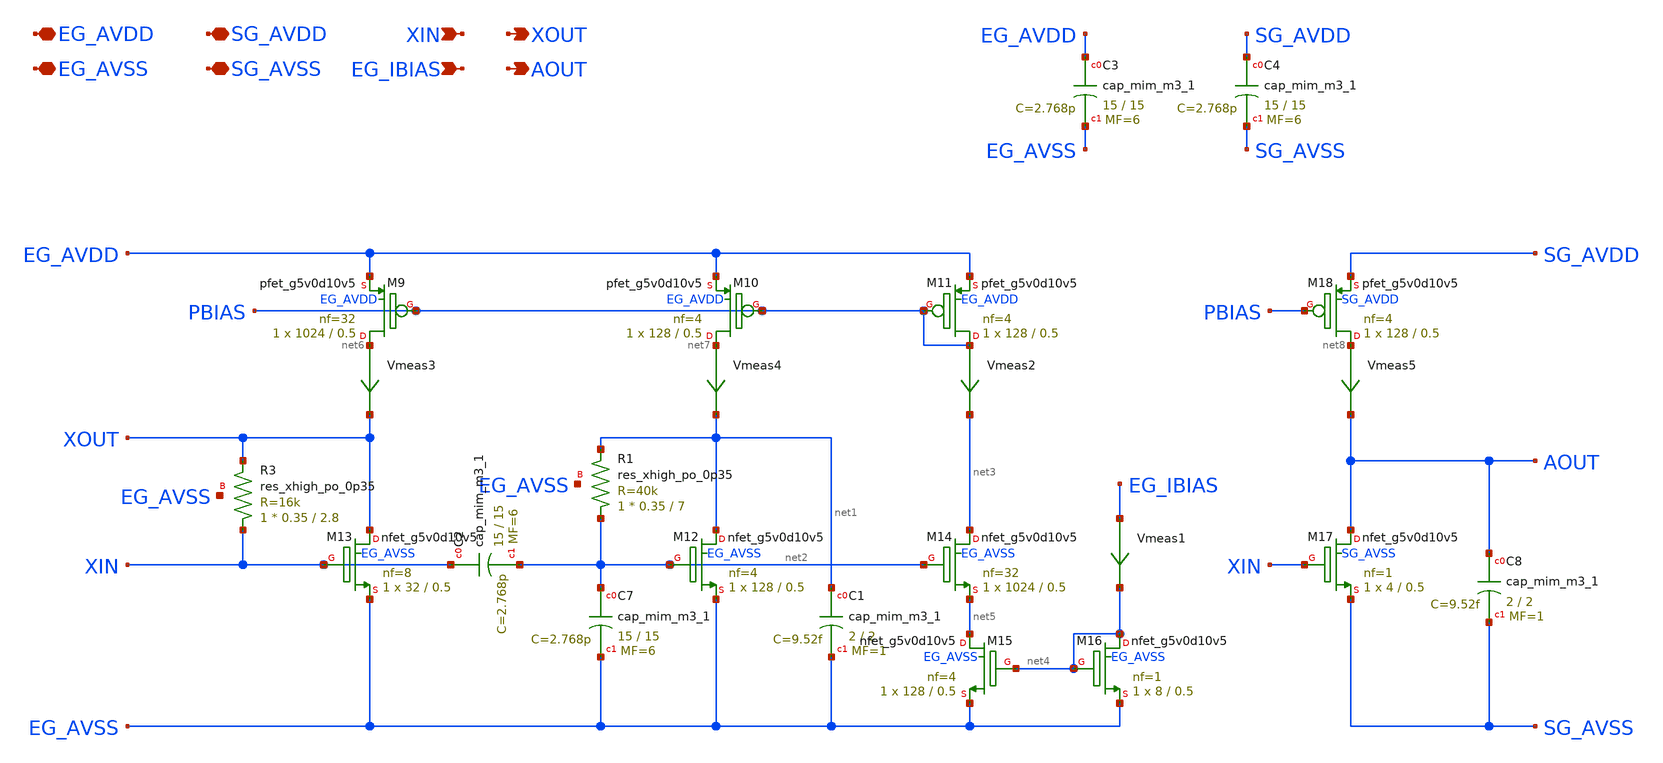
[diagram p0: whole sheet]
** sch_path: xschem/vittoz_pierce_osc.sch
**.subckt vittoz_pierce_osc EG_AVDD EG_AVSS SG_AVDD SG_AVSS XIN EG_IBIAS XOUT AOUT
*.iopin EG_AVDD
*.iopin EG_AVSS
*.iopin SG_AVDD
*.iopin SG_AVSS
*.ipin XIN
*.ipin EG_IBIAS
*.opin XOUT
*.opin AOUT
XM9 net6 PBIAS EG_AVDD EG_AVDD sky130_fd_pr__pfet_g5v0d10v5 L=0.5 W=1024 nf=32 ad='int((nf+1)/2) * W/nf * 0.29'
+ as='int((nf+2)/2) * W/nf * 0.29' pd='2*int((nf+1)/2) * (W/nf + 0.29)' ps='2*int((nf+2)/2) * (W/nf + 0.29)'
+ nrd='0.29 / W' nrs='0.29 / W' sa=0 sb=0 sd=0 mult=1 m=1
XM10 net7 PBIAS EG_AVDD EG_AVDD sky130_fd_pr__pfet_g5v0d10v5 L=0.5 W=128 nf=4 ad='int((nf+1)/2) * W/nf * 0.29'
+ as='int((nf+2)/2) * W/nf * 0.29' pd='2*int((nf+1)/2) * (W/nf + 0.29)' ps='2*int((nf+2)/2) * (W/nf + 0.29)'
+ nrd='0.29 / W' nrs='0.29 / W' sa=0 sb=0 sd=0 mult=1 m=1
XM11 PBIAS PBIAS EG_AVDD EG_AVDD sky130_fd_pr__pfet_g5v0d10v5 L=0.5 W=128 nf=4 ad='int((nf+1)/2) * W/nf * 0.29'
+ as='int((nf+2)/2) * W/nf * 0.29' pd='2*int((nf+1)/2) * (W/nf + 0.29)' ps='2*int((nf+2)/2) * (W/nf + 0.29)'
+ nrd='0.29 / W' nrs='0.29 / W' sa=0 sb=0 sd=0 mult=1 m=1
Vmeas3 net6 XOUT 0
.save i(vmeas3)
Vmeas4 net7 net1 0
.save i(vmeas4)
Vmeas2 PBIAS net3 0
.save i(vmeas2)
XM12 net1 net2 EG_AVSS EG_AVSS sky130_fd_pr__nfet_g5v0d10v5 L=0.5 W=128 nf=4 ad='int((nf+1)/2) * W/nf * 0.29'
+ as='int((nf+2)/2) * W/nf * 0.29' pd='2*int((nf+1)/2) * (W/nf + 0.29)' ps='2*int((nf+2)/2) * (W/nf + 0.29)'
+ nrd='0.29 / W' nrs='0.29 / W' sa=0 sb=0 sd=0 mult=1 m=1
XR1 net2 net1 EG_AVSS sky130_fd_pr__res_xhigh_po_0p35 L=7 mult=1 m=1
XC1 net1 EG_AVSS sky130_fd_pr__cap_mim_m3_1 W=2 L=2 MF=1 m=1
XC2 XIN net2 sky130_fd_pr__cap_mim_m3_1 W=15 L=15 MF=6 m=6
XC7 net2 EG_AVSS sky130_fd_pr__cap_mim_m3_1 W=15 L=15 MF=6 m=6
XM13 XOUT XIN EG_AVSS EG_AVSS sky130_fd_pr__nfet_g5v0d10v5 L=0.5 W=32 nf=8 ad='int((nf+1)/2) * W/nf * 0.29'
+ as='int((nf+2)/2) * W/nf * 0.29' pd='2*int((nf+1)/2) * (W/nf + 0.29)' ps='2*int((nf+2)/2) * (W/nf + 0.29)'
+ nrd='0.29 / W' nrs='0.29 / W' sa=0 sb=0 sd=0 mult=1 m=1
XM14 net3 net2 net5 EG_AVSS sky130_fd_pr__nfet_g5v0d10v5 L=0.5 W=1024 nf=32 ad='int((nf+1)/2) * W/nf * 0.29'
+ as='int((nf+2)/2) * W/nf * 0.29' pd='2*int((nf+1)/2) * (W/nf + 0.29)' ps='2*int((nf+2)/2) * (W/nf + 0.29)'
+ nrd='0.29 / W' nrs='0.29 / W' sa=0 sb=0 sd=0 mult=1 m=1
XM15 net5 net4 EG_AVSS EG_AVSS sky130_fd_pr__nfet_g5v0d10v5 L=0.5 W=128 nf=4 ad='int((nf+1)/2) * W/nf * 0.29'
+ as='int((nf+2)/2) * W/nf * 0.29' pd='2*int((nf+1)/2) * (W/nf + 0.29)' ps='2*int((nf+2)/2) * (W/nf + 0.29)'
+ nrd='0.29 / W' nrs='0.29 / W' sa=0 sb=0 sd=0 mult=1 m=1
XM16 net4 net4 EG_AVSS EG_AVSS sky130_fd_pr__nfet_g5v0d10v5 L=0.5 W=8 nf=1 ad='int((nf+1)/2) * W/nf * 0.29'
+ as='int((nf+2)/2) * W/nf * 0.29' pd='2*int((nf+1)/2) * (W/nf + 0.29)' ps='2*int((nf+2)/2) * (W/nf + 0.29)'
+ nrd='0.29 / W' nrs='0.29 / W' sa=0 sb=0 sd=0 mult=1 m=1
XR3 XIN XOUT EG_AVSS sky130_fd_pr__res_xhigh_po_0p35 L=2.8 mult=1 m=1
XM17 AOUT XIN SG_AVSS SG_AVSS sky130_fd_pr__nfet_g5v0d10v5 L=0.5 W=4 nf=1 ad='int((nf+1)/2) * W/nf * 0.29'
+ as='int((nf+2)/2) * W/nf * 0.29' pd='2*int((nf+1)/2) * (W/nf + 0.29)' ps='2*int((nf+2)/2) * (W/nf + 0.29)'
+ nrd='0.29 / W' nrs='0.29 / W' sa=0 sb=0 sd=0 mult=1 m=1
XM18 net8 PBIAS SG_AVDD SG_AVDD sky130_fd_pr__pfet_g5v0d10v5 L=0.5 W=128 nf=4 ad='int((nf+1)/2) * W/nf * 0.29'
+ as='int((nf+2)/2) * W/nf * 0.29' pd='2*int((nf+1)/2) * (W/nf + 0.29)' ps='2*int((nf+2)/2) * (W/nf + 0.29)'
+ nrd='0.29 / W' nrs='0.29 / W' sa=0 sb=0 sd=0 mult=1 m=1
Vmeas5 net8 AOUT 0
.save i(vmeas5)
XC8 AOUT SG_AVSS sky130_fd_pr__cap_mim_m3_1 W=2 L=2 MF=1 m=1
XC3 EG_AVDD EG_AVSS sky130_fd_pr__cap_mim_m3_1 W=15 L=15 MF=6 m=6
XC4 SG_AVDD SG_AVSS sky130_fd_pr__cap_mim_m3_1 W=15 L=15 MF=6 m=6
Vmeas1 EG_IBIAS net4 0
.save i(vmeas1)
**.ends
.end
